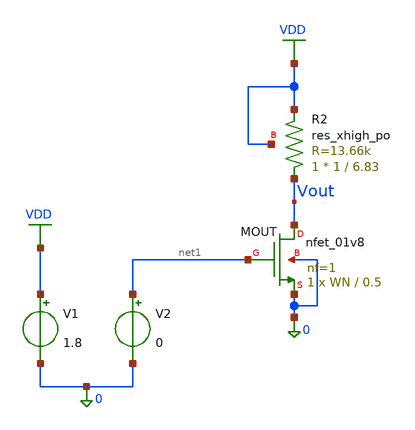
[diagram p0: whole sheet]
** sch_path: designs_backup/designs/test_cir.sch
**.subckt test_cir
XMOUT Vout net1 0 0 sky130_fd_pr__nfet_01v8 L=0.5 W=WN nf=1 ad='int((1 + 1)/2) * WN / 1 * 0.29' as='int((1 + 2)/2) * WN / 1 * 0.29'
+ pd='2*int((1 + 1)/2) * (WN / 1 + 0.29)' ps='2*int((1 + 2)/2) * (WN / 1 + 0.29)' nrd='0.29 / WN ' nrs='0.29 / WN '
+ sa=0 sb=0 sd=0 mult=1 m=1
V1 VDD 0 1.8
V2 net1 0 0
XR2 Vout VDD VDD sky130_fd_pr__res_xhigh_po W=1 L=6.83 mult=1 m=1
**** begin user architecture code


* ngspice commands
.param WN=1
.options savecurrents
.dc v2 0 1.8 0.01
.control
  let start_w = 1
  let stop_w = 90
  let delta_w = 5
  let w_act = start_w
  let new_vth = 0.3
  while w_act le stop_w
    alterparam WN = $&w_act
    reset
    ** example for changing a model param
    * altermod @m.xm1.msky130_fd_pr__nfet_01v8[vth0]=$&new_vth
    save all
    save @m.xm1.msky130_fd_pr__nfet_01v8[id]
    save @m.xm1.msky130_fd_pr__nfet_01v8[gm]
    save @m.xm1.msky130_fd_pr__nfet_01v8[W]
    run
    remzerovec
    write /foss/designs/simulations/test_sweep_nmos_w.raw
    let w_act = w_act + delta_w
    set appendwrite
  end
  load /foss/designs/simulations/test_sweep_mos_w.raw
  plot dc1.v(vout)
  plot dc1.@m.xmout.msky130_fd_pr__nfet_01v8[id]
  print dc1.@m.xmout.msky130_fd_pr__nfet_01v8[gm]
.endc



** opencircuitdesign pdks install
.lib $::SKYWATER_MODELS/sky130.lib.spice tt

**** end user architecture code
**.ends
.GLOBAL VDD
.end
